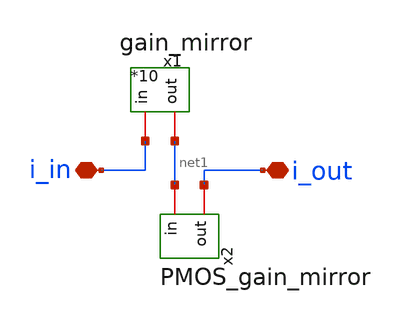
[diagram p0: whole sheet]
** sch_path: schemas/INPUT_AMP.sch
**.subckt INPUT_AMP i_out i_in
*.iopin i_out
*.iopin i_in
x1 net1 i_in gain_mirror
x2 i_out net1 PMOS_gain_mirror
**.ends

* expanding   symbol:  /home/lxbtlr/DTILO/schemas/gain_mirror.sym # of pins=2
** sym_path: schemas/gain_mirror.sym
** sch_path: schemas/gain_mirror.sch
.subckt gain_mirror out in
*.iopin in
*.iopin out
XM1 in in GND GND sky130_fd_pr__nfet_01v8 L={L} W={W} nf=1 ad='int((nf+1)/2) * W/nf * 0.29' as='int((nf+2)/2) * W/nf * 0.29'
+ pd='2*int((nf+1)/2) * (W/nf + 0.29)' ps='2*int((nf+2)/2) * (W/nf + 0.29)' nrd='0.29 / W' nrs='0.29 / W'
+ sa=0 sb=0 sd=0 mult=1 m=1
XM2 out in GND GND sky130_fd_pr__nfet_01v8 L={L} W={W} nf=1 ad='int((nf+1)/2) * W/nf * 0.29' as='int((nf+2)/2) * W/nf * 0.29'
+ pd='2*int((nf+1)/2) * (W/nf + 0.29)' ps='2*int((nf+2)/2) * (W/nf + 0.29)' nrd='0.29 / W' nrs='0.29 / W'
+ sa=0 sb=0 sd=0 mult={M_amp} m={M_amp}
XM3 out in GND GND sky130_fd_pr__nfet_01v8 L={L} W={W} nf=1 ad='int((nf+1)/2) * W/nf * 0.29' as='int((nf+2)/2) * W/nf * 0.29'
+ pd='2*int((nf+1)/2) * (W/nf + 0.29)' ps='2*int((nf+2)/2) * (W/nf + 0.29)' nrd='0.29 / W' nrs='0.29 / W'
+ sa=0 sb=0 sd=0 mult={M_amp} m={M_amp}
XM4 out in GND GND sky130_fd_pr__nfet_01v8 L={L} W={W} nf=1 ad='int((nf+1)/2) * W/nf * 0.29' as='int((nf+2)/2) * W/nf * 0.29'
+ pd='2*int((nf+1)/2) * (W/nf + 0.29)' ps='2*int((nf+2)/2) * (W/nf + 0.29)' nrd='0.29 / W' nrs='0.29 / W'
+ sa=0 sb=0 sd=0 mult={M_amp} m={M_amp}
XM5 out in GND GND sky130_fd_pr__nfet_01v8 L={L} W={W} nf=1 ad='int((nf+1)/2) * W/nf * 0.29' as='int((nf+2)/2) * W/nf * 0.29'
+ pd='2*int((nf+1)/2) * (W/nf + 0.29)' ps='2*int((nf+2)/2) * (W/nf + 0.29)' nrd='0.29 / W' nrs='0.29 / W'
+ sa=0 sb=0 sd=0 mult={M_amp} m={M_amp}
XM6 out in GND GND sky130_fd_pr__nfet_01v8 L={L} W={W} nf=1 ad='int((nf+1)/2) * W/nf * 0.29' as='int((nf+2)/2) * W/nf * 0.29'
+ pd='2*int((nf+1)/2) * (W/nf + 0.29)' ps='2*int((nf+2)/2) * (W/nf + 0.29)' nrd='0.29 / W' nrs='0.29 / W'
+ sa=0 sb=0 sd=0 mult={M_amp} m={M_amp}
.ends


* expanding   symbol:  /home/lxbtlr/DTILO/schemas/PMOS_gain_mirror.sym # of pins=2
** sym_path: schemas/PMOS_gain_mirror.sym
** sch_path: schemas/PMOS_gain_mirror.sch
.subckt PMOS_gain_mirror out in
*.iopin in
*.iopin out
XM1 in in VDD VDD sky130_fd_pr__pfet_01v8 L={L} W={W} nf=1 ad='int((nf+1)/2) * W/nf * 0.29' as='int((nf+2)/2) * W/nf * 0.29'
+ pd='2*int((nf+1)/2) * (W/nf + 0.29)' ps='2*int((nf+2)/2) * (W/nf + 0.29)' nrd='0.29 / W' nrs='0.29 / W'
+ sa=0 sb=0 sd=0 mult=1 m=1
XM2 out in VDD VDD sky130_fd_pr__pfet_01v8 L={L} W={W} nf=1 ad='int((nf+1)/2) * W/nf * 0.29' as='int((nf+2)/2) * W/nf * 0.29'
+ pd='2*int((nf+1)/2) * (W/nf + 0.29)' ps='2*int((nf+2)/2) * (W/nf + 0.29)' nrd='0.29 / W' nrs='0.29 / W'
+ sa=0 sb=0 sd=0 mult={M_amp} m={M_amp}
XM3 out in VDD VDD sky130_fd_pr__pfet_01v8 L={L} W={W} nf=1 ad='int((nf+1)/2) * W/nf * 0.29' as='int((nf+2)/2) * W/nf * 0.29'
+ pd='2*int((nf+1)/2) * (W/nf + 0.29)' ps='2*int((nf+2)/2) * (W/nf + 0.29)' nrd='0.29 / W' nrs='0.29 / W'
+ sa=0 sb=0 sd=0 mult={M_amp} m={M_amp}
XM4 out in VDD VDD sky130_fd_pr__pfet_01v8 L={L} W={W} nf=1 ad='int((nf+1)/2) * W/nf * 0.29' as='int((nf+2)/2) * W/nf * 0.29'
+ pd='2*int((nf+1)/2) * (W/nf + 0.29)' ps='2*int((nf+2)/2) * (W/nf + 0.29)' nrd='0.29 / W' nrs='0.29 / W'
+ sa=0 sb=0 sd=0 mult={M_amp} m={M_amp}
XM5 out in VDD VDD sky130_fd_pr__pfet_01v8 L={L} W={W} nf=1 ad='int((nf+1)/2) * W/nf * 0.29' as='int((nf+2)/2) * W/nf * 0.29'
+ pd='2*int((nf+1)/2) * (W/nf + 0.29)' ps='2*int((nf+2)/2) * (W/nf + 0.29)' nrd='0.29 / W' nrs='0.29 / W'
+ sa=0 sb=0 sd=0 mult={M_amp} m={M_amp}
XM6 out in VDD VDD sky130_fd_pr__pfet_01v8 L={L} W={W} nf=1 ad='int((nf+1)/2) * W/nf * 0.29' as='int((nf+2)/2) * W/nf * 0.29'
+ pd='2*int((nf+1)/2) * (W/nf + 0.29)' ps='2*int((nf+2)/2) * (W/nf + 0.29)' nrd='0.29 / W' nrs='0.29 / W'
+ sa=0 sb=0 sd=0 mult={M_amp} m={M_amp}
.ends

.GLOBAL GND
.GLOBAL VDD
.end
